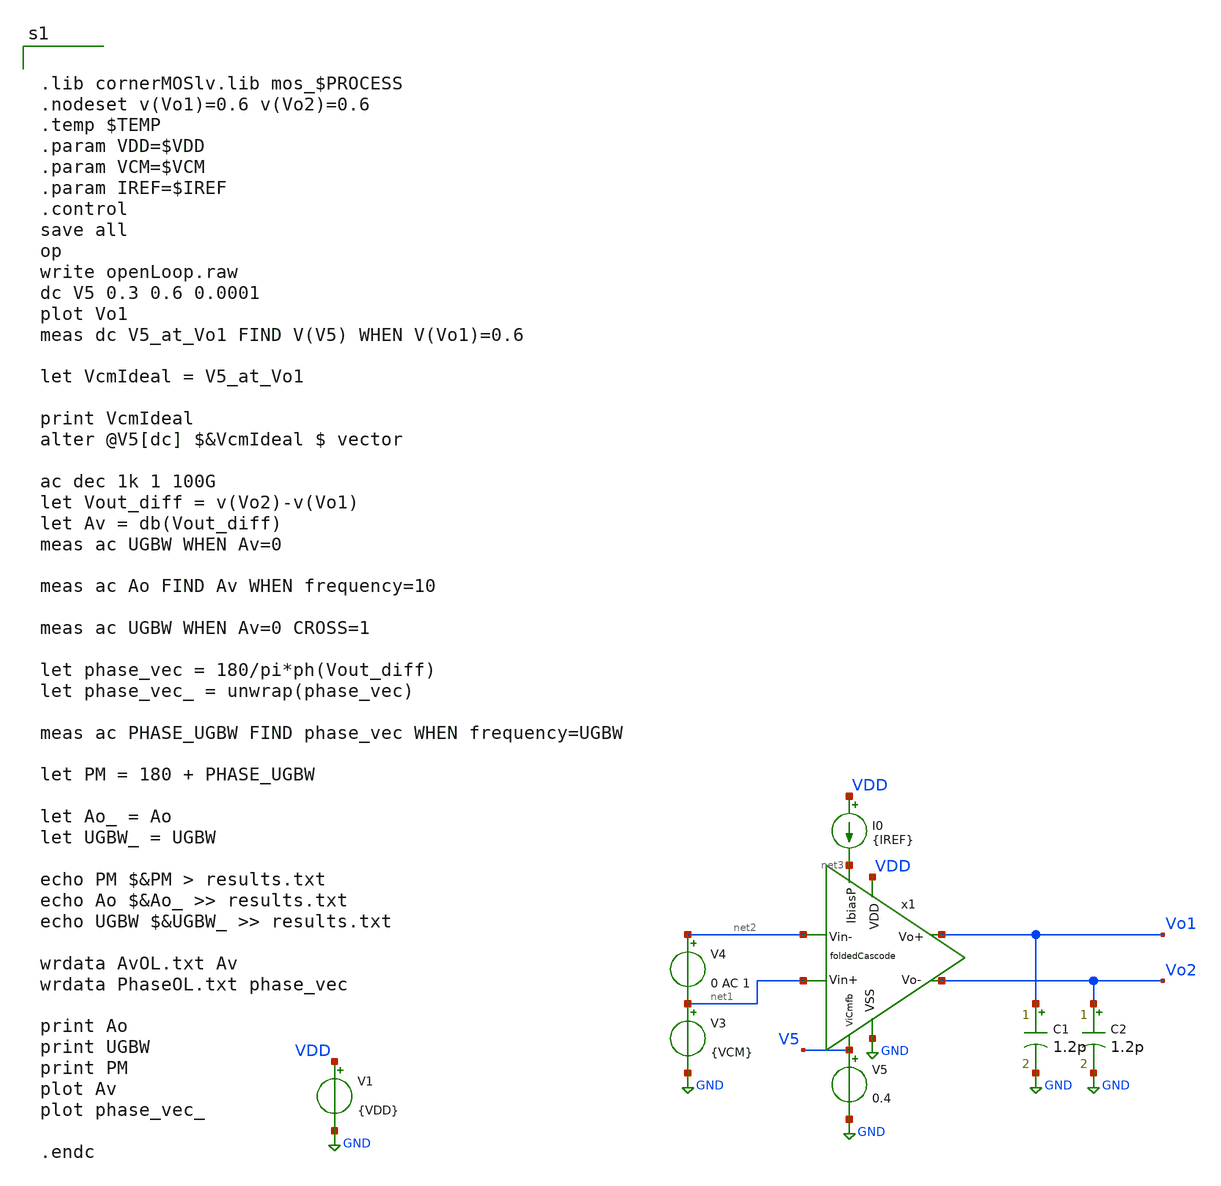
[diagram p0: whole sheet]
** sch_path: sch/AutoTestbench/tb/done/openLoop.sch
**.subckt openLoop
x1 VDD GND V5 net3 Vo1 Vo2 net2 net1 foldedCascode
V1 VDD GND {VDD}
V3 net1 GND {VCM}
V4 net2 net1 0 AC 1
C1 Vo1 GND 1.2p m=1
C2 Vo2 GND 1.2p m=1
V5 V5 GND 0.4
I0 VDD net3 {IREF}
**** begin user architecture code


.lib cornerMOSlv.lib mos_$PROCESS
.nodeset v(Vo1)=0.6 v(Vo2)=0.6
.temp $TEMP
.param VDD=$VDD
.param VCM=$VCM
.param IREF=$IREF
.control
save all
op
write openLoop.raw
dc V5 0.3 0.6 0.0001
plot Vo1
meas dc V5_at_Vo1 FIND V(V5) WHEN V(Vo1)=0.6

let VcmIdeal = V5_at_Vo1

print VcmIdeal
alter @V5[dc] $&VcmIdeal $ vector

ac dec 1k 1 100G
let Vout_diff = v(Vo2)-v(Vo1)
let Av = db(Vout_diff)
meas ac UGBW WHEN Av=0

meas ac Ao FIND Av WHEN frequency=10

meas ac UGBW WHEN Av=0 CROSS=1

let phase_vec = 180/pi*ph(Vout_diff)
let phase_vec_ = unwrap(phase_vec)

meas ac PHASE_UGBW FIND phase_vec WHEN frequency=UGBW

let PM = 180 + PHASE_UGBW

let Ao_ = Ao
let UGBW_ = UGBW

echo PM $&PM > results.txt
echo Ao $&Ao_ >> results.txt
echo UGBW $&UGBW_ >> results.txt

wrdata AvOL.txt Av
wrdata PhaseOL.txt phase_vec

print Ao
print UGBW
print PM
plot Av
plot phase_vec_

.endc


**** end user architecture code
**.ends

* expanding   symbol:  foldedCascode.sym # of pins=8
** sym_path: sch/blocks/foldedCascode.sym
** sch_path: sch/blocks/foldedCascode.sch
.subckt foldedCascode VDD VSS ViCmfb IbiasP Vo+ Vo- Vin- Vin+
*.iopin VSS
*.iopin VDD
*.ipin ViCmfb
*.iopin IbiasP
*.ipin Vin+
*.ipin Vin-
*.iopin Vo+
*.iopin Vo-
x1 VDD Vb1_1 Vb1_2 Vx Vy VSS gmBoosting
XM0 net3 Vb0 VDD VDD sg13_lv_pmos w=70u l=0.3u ng=120 m=8 mm_ok=1
XM1 Vy Vin+ net3 net3 sg13_lv_pmos w=85u l=0.13u ng=100 m=2 mm_ok=1
XM2 Vx Vin- net3 net3 sg13_lv_pmos w=85u l=0.13u ng=100 m=2 mm_ok=1
XM7 Vo+ Vb2 net1 VDD sg13_lv_pmos w=47u l=0.4u ng=94 m=4 mm_ok=1
XM3 Vo+ Vb1_1 Vx VSS sg13_lv_nmos w=44u l=0.3u ng=22 m=6 mm_ok=1
XM8 Vo- Vb2 net2 VDD sg13_lv_pmos w=47u l=0.4u ng=94 m=4 mm_ok=1
XM12 Vx ViCmfb VSS VSS sg13_lv_nmos w=24.3u l=0.8u ng=62 m=6 mm_ok=1
XM4 Vo- Vb1_2 Vy VSS sg13_lv_nmos w=44u l=0.3u ng=22 m=6 mm_ok=1
XM5 Vy ViCmfb VSS VSS sg13_lv_nmos w=24.3u l=0.8u ng=62 m=6 mm_ok=1
I0 Vb0 VSS 10u
XM6 Vb0 Vb0 net4 VDD sg13_lv_pmos w=60u l=0.13u ng=10 m=1 mm_ok=1
XM13 net4 Vb0 VDD VDD sg13_lv_pmos w=11.5u l=0.3u ng=5 m=1 mm_ok=1
I1 Vb2 VSS 25u
XM18 Vb2 Vb2 net5 VDD sg13_lv_pmos w=18.5u l=0.7u ng=9 m=1 mm_ok=1
XM19 net5 Vb2 VDD VDD sg13_lv_pmos w=4u l=0.7u ng=1 m=1 mm_ok=1
XM20 Vb3 Vb2 net6 VDD sg13_lv_pmos w=5.5u l=0.4u ng=1 m=1 mm_ok=1
XM21 net6 Vb3 VDD VDD sg13_lv_pmos w=8.1u l=0.8u ng=1 m=1 mm_ok=1
I2 Vb3 VSS 10u
XM11 IbiasP IbiasP VSS VSS sg13_lv_nmos w=44u l=0.3u ng=22 m=6 mm_ok=1
XM9 net1 Vb3 VDD VDD sg13_lv_pmos w=62.2u l=0.8u ng=118 m=4 mm_ok=1
XM10 net2 Vb3 VDD VDD sg13_lv_pmos w=62.2u l=0.8u ng=118 m=4 mm_ok=1
.ends


* expanding   symbol:  gmBoosting.sym # of pins=6
** sym_path: sch/blocks/gmBoosting.sym
** sch_path: sch/blocks/gmBoosting.sch
.subckt gmBoosting VDD Vo2 Vo1 Vi+ Vi- VSS
*.iopin VSS
*.opin Vo1
*.opin Vo2
*.ipin Vi+
*.ipin Vi-
*.iopin VDD
V1 Vref VSS 0.55
XM7 net2 Vb4 VDD VDD sg13_lv_pmos w=25u l=0.7u ng=13 m=2 mm_ok=1
XM1 net8 Vi+ net1 net1 sg13_lv_pmos w=40u l=0.15u ng=80 m=4 mm_ok=1
XM2 net4 Vi- net1 net1 sg13_lv_pmos w=40u l=0.15u ng=80 m=4 mm_ok=1
XM0 net1 Vb0 net5 VDD sg13_lv_pmos w=16u l=0.3u ng=20 m=1 mm_ok=1
XM6 net8 Vb3 VSS VSS sg13_lv_nmos w=20u l=0.7u ng=5 m=2 mm_ok=1
XM9 Vo1 Vb2 net2 VDD sg13_lv_pmos w=30u l=0.3u ng=10 m=1 mm_ok=1
XM10 Vo2 Vb2 net3 VDD sg13_lv_pmos w=30u l=0.3u ng=10 m=1 mm_ok=1
XM8 net3 Vb4 VDD VDD sg13_lv_pmos w=25u l=0.7u ng=13 m=2 mm_ok=1
XM3 net5 Vo2 VDD VDD sg13_lv_pmos w=20u l=0.13u ng=5 m=1 mm_ok=1
XM4 net5 Vo1 VDD VDD sg13_lv_pmos w=20u l=0.13u ng=5 m=1 mm_ok=1
XM5 net6 Vref VDD VDD sg13_lv_pmos w=20u l=0.13u ng=5 m=2 mm_ok=1
XM28 Vb0 net7 VSS VSS sg13_lv_nmos w=10u l=0.2u ng=2 m=1 mm_ok=1
XM29 Vb3 Vb3 VSS VSS sg13_lv_nmos w=30u l=0.2u ng=4 m=1 mm_ok=1
XR16 net7 Vb0 sub! rppd w=0.8e-6 l=2.5e-6 m=1 b=0 mm_ok=1
XM30 Vb3 Vb0 net6 VDD sg13_lv_pmos w=16u l=0.3u ng=20 m=1 mm_ok=1
XM31 net4 Vb3 VSS VSS sg13_lv_nmos w=20u l=0.7u ng=5 m=2 mm_ok=1
XM32 Vo1 Vb1 net4 VSS sg13_lv_nmos w=37.5u l=0.7u ng=5 m=1 mm_ok=1
XM33 Vo2 Vb1 net8 VSS sg13_lv_nmos w=37.5u l=0.7u ng=5 m=1 mm_ok=1
XM23 net7 Vbb VDD VDD sg13_lv_pmos w=18u l=1u ng=18 m=1 mm_ok=1
XR9 Vb1 net10 sub! rhigh w=0.5e-6 l=2.31e-6 m=1 b=0 mm_ok=1
XM17 net10 Vb1 net9 VSS sg13_lv_nmos w=25u l=0.7u ng=3 m=1 mm_ok=1
XM18 net9 net10 VSS VSS sg13_lv_nmos w=40u l=0.7u ng=4 m=1 mm_ok=1
XM19 net11 Vb4 VDD VDD sg13_lv_pmos w=15u l=0.7u ng=5 m=1 mm_ok=1
XM20 Vb4 Vb2 net11 VDD sg13_lv_pmos w=7u l=0.3u ng=7 m=1 mm_ok=1
XR10 Vb4 Vb2 sub! rhigh w=0.5e-6 l=1.8e-6 m=1 b=0 mm_ok=1
I3 Vbb VSS 50u
XM21 Vbb Vbb VDD VDD sg13_lv_pmos w=18u l=1u ng=18 m=1 mm_ok=1
XM22 Vb1 Vbb VDD VDD sg13_lv_pmos w=18u l=1u ng=18 m=1 mm_ok=1
XM24 net12 Vbb VDD VDD sg13_lv_pmos w=18u l=1u ng=18 m=1 mm_ok=1
XM25 net12 net12 VSS VSS sg13_lv_nmos w=15u l=1u ng=2 m=1 mm_ok=1
XM26 Vb2 net12 VSS VSS sg13_lv_nmos w=15u l=1u ng=2 m=1 mm_ok=1
.ends

.GLOBAL GND
.end
